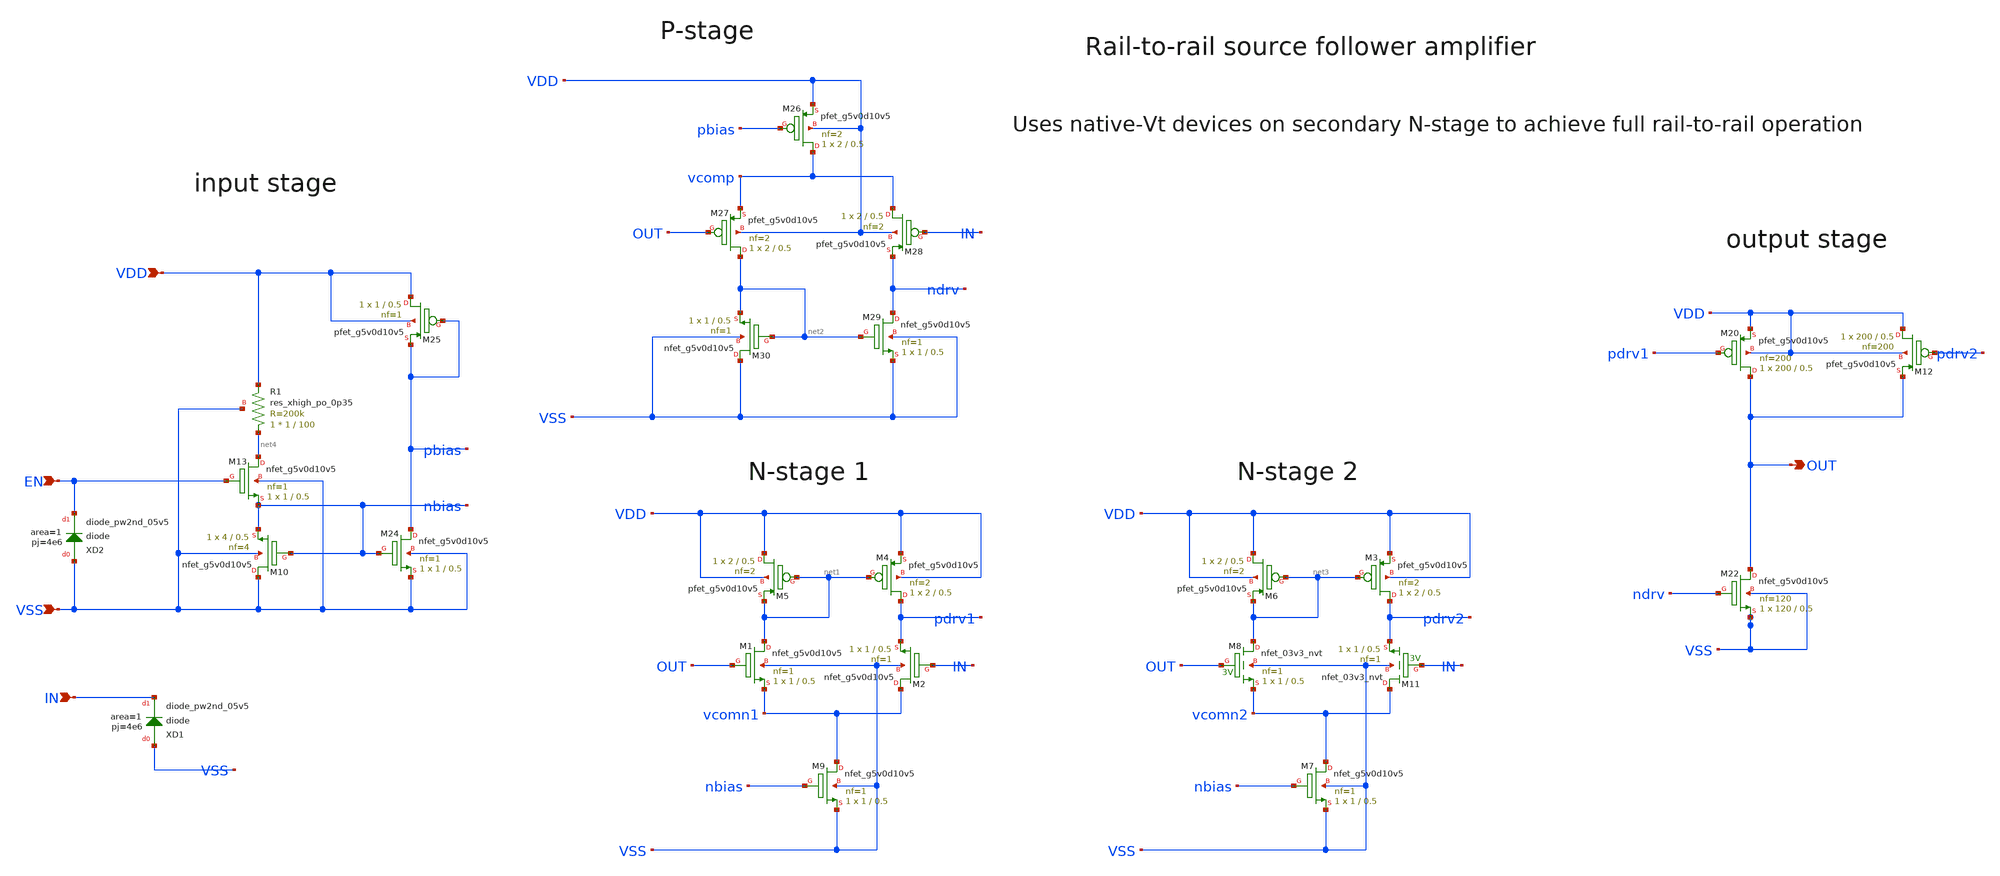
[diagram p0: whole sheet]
** sch_path: spice/xschem/EF_BUF3V3p.sch
**.subckt EF_BUF3V3p IN VDD VSS OUT EN
*.ipin IN
*.ipin VDD
*.ipin VSS
*.opin OUT
*.ipin EN
XM4 pdrv1 net1 VDD VDD sky130_fd_pr__pfet_g5v0d10v5 L=0.5 W=2 nf=2 ad='int((nf+1)/2) * W/nf * 0.29' as='int((nf+2)/2) * W/nf * 0.29'
+ pd='2*int((nf+1)/2) * (W/nf + 0.29)' ps='2*int((nf+2)/2) * (W/nf + 0.29)' nrd='0.29 / W' nrs='0.29 / W'
+ sa=0 sb=0 sd=0 mult=1 m=1
XM5 VDD net1 net1 VDD sky130_fd_pr__pfet_g5v0d10v5 L=0.5 W=2 nf=2 ad='int((nf+1)/2) * W/nf * 0.29' as='int((nf+2)/2) * W/nf * 0.29'
+ pd='2*int((nf+1)/2) * (W/nf + 0.29)' ps='2*int((nf+2)/2) * (W/nf + 0.29)' nrd='0.29 / W' nrs='0.29 / W'
+ sa=0 sb=0 sd=0 mult=1 m=1
XM9 vcomn1 nbias VSS VSS sky130_fd_pr__nfet_g5v0d10v5 L=0.5 W=1 nf=1 ad='int((nf+1)/2) * W/nf * 0.29'
+ as='int((nf+2)/2) * W/nf * 0.29' pd='2*int((nf+1)/2) * (W/nf + 0.29)' ps='2*int((nf+2)/2) * (W/nf + 0.29)'
+ nrd='0.29 / W' nrs='0.29 / W' sa=0 sb=0 sd=0 mult=1 m=1
XM10 VSS nbias nbias VSS sky130_fd_pr__nfet_g5v0d10v5 L=0.5 W=4 nf=4 ad='int((nf+1)/2) * W/nf * 0.29'
+ as='int((nf+2)/2) * W/nf * 0.29' pd='2*int((nf+1)/2) * (W/nf + 0.29)' ps='2*int((nf+2)/2) * (W/nf + 0.29)'
+ nrd='0.29 / W' nrs='0.29 / W' sa=0 sb=0 sd=0 mult=1 m=1
XR1 net4 VDD VSS sky130_fd_pr__res_xhigh_po_0p35 W=1 L=100 mult=1 m=1
XM20 OUT pdrv1 VDD VDD sky130_fd_pr__pfet_g5v0d10v5 L=0.5 W=200 nf=200 ad='int((nf+1)/2) * W/nf * 0.29'
+ as='int((nf+2)/2) * W/nf * 0.29' pd='2*int((nf+1)/2) * (W/nf + 0.29)' ps='2*int((nf+2)/2) * (W/nf + 0.29)'
+ nrd='0.29 / W' nrs='0.29 / W' sa=0 sb=0 sd=0 mult=1 m=1
XM22 OUT ndrv VSS VSS sky130_fd_pr__nfet_g5v0d10v5 L=0.5 W=120 nf=120 ad='int((nf+1)/2) * W/nf * 0.29'
+ as='int((nf+2)/2) * W/nf * 0.29' pd='2*int((nf+1)/2) * (W/nf + 0.29)' ps='2*int((nf+2)/2) * (W/nf + 0.29)'
+ nrd='0.29 / W' nrs='0.29 / W' sa=0 sb=0 sd=0 mult=1 m=1
XM24 pbias nbias VSS VSS sky130_fd_pr__nfet_g5v0d10v5 L=0.5 W=1 nf=1 ad='int((nf+1)/2) * W/nf * 0.29'
+ as='int((nf+2)/2) * W/nf * 0.29' pd='2*int((nf+1)/2) * (W/nf + 0.29)' ps='2*int((nf+2)/2) * (W/nf + 0.29)'
+ nrd='0.29 / W' nrs='0.29 / W' sa=0 sb=0 sd=0 mult=1 m=1
XM25 VDD pbias pbias VDD sky130_fd_pr__pfet_g5v0d10v5 L=0.5 W=1 nf=1 ad='int((nf+1)/2) * W/nf * 0.29'
+ as='int((nf+2)/2) * W/nf * 0.29' pd='2*int((nf+1)/2) * (W/nf + 0.29)' ps='2*int((nf+2)/2) * (W/nf + 0.29)'
+ nrd='0.29 / W' nrs='0.29 / W' sa=0 sb=0 sd=0 mult=1 m=1
XM26 vcomp pbias VDD VDD sky130_fd_pr__pfet_g5v0d10v5 L=0.5 W=2 nf=2 ad='int((nf+1)/2) * W/nf * 0.29'
+ as='int((nf+2)/2) * W/nf * 0.29' pd='2*int((nf+1)/2) * (W/nf + 0.29)' ps='2*int((nf+2)/2) * (W/nf + 0.29)'
+ nrd='0.29 / W' nrs='0.29 / W' sa=0 sb=0 sd=0 mult=1 m=1
XM27 net2 OUT vcomp VDD sky130_fd_pr__pfet_g5v0d10v5 L=0.5 W=2 nf=2 ad='int((nf+1)/2) * W/nf * 0.29'
+ as='int((nf+2)/2) * W/nf * 0.29' pd='2*int((nf+1)/2) * (W/nf + 0.29)' ps='2*int((nf+2)/2) * (W/nf + 0.29)'
+ nrd='0.29 / W' nrs='0.29 / W' sa=0 sb=0 sd=0 mult=1 m=1
XM28 vcomp IN ndrv VDD sky130_fd_pr__pfet_g5v0d10v5 L=0.5 W=2 nf=2 ad='int((nf+1)/2) * W/nf * 0.29' as='int((nf+2)/2) * W/nf * 0.29'
+ pd='2*int((nf+1)/2) * (W/nf + 0.29)' ps='2*int((nf+2)/2) * (W/nf + 0.29)' nrd='0.29 / W' nrs='0.29 / W'
+ sa=0 sb=0 sd=0 mult=1 m=1
XM29 ndrv net2 VSS VSS sky130_fd_pr__nfet_g5v0d10v5 L=0.5 W=1 nf=1 ad='int((nf+1)/2) * W/nf * 0.29' as='int((nf+2)/2) * W/nf * 0.29'
+ pd='2*int((nf+1)/2) * (W/nf + 0.29)' ps='2*int((nf+2)/2) * (W/nf + 0.29)' nrd='0.29 / W' nrs='0.29 / W'
+ sa=0 sb=0 sd=0 mult=1 m=1
XM30 VSS net2 net2 VSS sky130_fd_pr__nfet_g5v0d10v5 L=0.5 W=1 nf=1 ad='int((nf+1)/2) * W/nf * 0.29' as='int((nf+2)/2) * W/nf * 0.29'
+ pd='2*int((nf+1)/2) * (W/nf + 0.29)' ps='2*int((nf+2)/2) * (W/nf + 0.29)' nrd='0.29 / W' nrs='0.29 / W'
+ sa=0 sb=0 sd=0 mult=1 m=1
XM1 net1 OUT vcomn1 VSS sky130_fd_pr__nfet_g5v0d10v5 L=0.5 W=1 nf=1 ad='int((nf+1)/2) * W/nf * 0.29'
+ as='int((nf+2)/2) * W/nf * 0.29' pd='2*int((nf+1)/2) * (W/nf + 0.29)' ps='2*int((nf+2)/2) * (W/nf + 0.29)'
+ nrd='0.29 / W' nrs='0.29 / W' sa=0 sb=0 sd=0 mult=1 m=1
XM2 vcomn1 IN pdrv1 VSS sky130_fd_pr__nfet_g5v0d10v5 L=0.5 W=1 nf=1 ad='int((nf+1)/2) * W/nf * 0.29'
+ as='int((nf+2)/2) * W/nf * 0.29' pd='2*int((nf+1)/2) * (W/nf + 0.29)' ps='2*int((nf+2)/2) * (W/nf + 0.29)'
+ nrd='0.29 / W' nrs='0.29 / W' sa=0 sb=0 sd=0 mult=1 m=1
XM3 pdrv2 net3 VDD VDD sky130_fd_pr__pfet_g5v0d10v5 L=0.5 W=2 nf=2 ad='int((nf+1)/2) * W/nf * 0.29' as='int((nf+2)/2) * W/nf * 0.29'
+ pd='2*int((nf+1)/2) * (W/nf + 0.29)' ps='2*int((nf+2)/2) * (W/nf + 0.29)' nrd='0.29 / W' nrs='0.29 / W'
+ sa=0 sb=0 sd=0 mult=1 m=1
XM6 VDD net3 net3 VDD sky130_fd_pr__pfet_g5v0d10v5 L=0.5 W=2 nf=2 ad='int((nf+1)/2) * W/nf * 0.29' as='int((nf+2)/2) * W/nf * 0.29'
+ pd='2*int((nf+1)/2) * (W/nf + 0.29)' ps='2*int((nf+2)/2) * (W/nf + 0.29)' nrd='0.29 / W' nrs='0.29 / W'
+ sa=0 sb=0 sd=0 mult=1 m=1
XM7 vcomn2 nbias VSS VSS sky130_fd_pr__nfet_g5v0d10v5 L=0.5 W=1 nf=1 ad='int((nf+1)/2) * W/nf * 0.29'
+ as='int((nf+2)/2) * W/nf * 0.29' pd='2*int((nf+1)/2) * (W/nf + 0.29)' ps='2*int((nf+2)/2) * (W/nf + 0.29)'
+ nrd='0.29 / W' nrs='0.29 / W' sa=0 sb=0 sd=0 mult=1 m=1
XM8 net3 OUT vcomn2 VSS sky130_fd_pr__nfet_03v3_nvt L=0.5 W=1 nf=1 ad='int((nf+1)/2) * W/nf * 0.29' as='int((nf+2)/2) * W/nf * 0.29'
+ pd='2*int((nf+1)/2) * (W/nf + 0.29)' ps='2*int((nf+2)/2) * (W/nf + 0.29)' nrd='0.29 / W' nrs='0.29 / W'
+ sa=0 sb=0 sd=0 mult=1 m=1
XM11 vcomn2 IN pdrv2 VSS sky130_fd_pr__nfet_03v3_nvt L=0.5 W=1 nf=1 ad='int((nf+1)/2) * W/nf * 0.29'
+ as='int((nf+2)/2) * W/nf * 0.29' pd='2*int((nf+1)/2) * (W/nf + 0.29)' ps='2*int((nf+2)/2) * (W/nf + 0.29)'
+ nrd='0.29 / W' nrs='0.29 / W' sa=0 sb=0 sd=0 mult=1 m=1
XM12 VDD pdrv2 OUT VDD sky130_fd_pr__pfet_g5v0d10v5 L=0.5 W=200 nf=200 ad='int((nf+1)/2) * W/nf * 0.29'
+ as='int((nf+2)/2) * W/nf * 0.29' pd='2*int((nf+1)/2) * (W/nf + 0.29)' ps='2*int((nf+2)/2) * (W/nf + 0.29)'
+ nrd='0.29 / W' nrs='0.29 / W' sa=0 sb=0 sd=0 mult=1 m=1
XXD1 VSS IN sky130_fd_pr__diode_pw2nd_05v5 area=1 pj=4e6
XM13 net4 EN nbias VSS sky130_fd_pr__nfet_g5v0d10v5 L=0.5 W=1 nf=1 ad='int((nf+1)/2) * W/nf * 0.29' as='int((nf+2)/2) * W/nf * 0.29'
+ pd='2*int((nf+1)/2) * (W/nf + 0.29)' ps='2*int((nf+2)/2) * (W/nf + 0.29)' nrd='0.29 / W' nrs='0.29 / W'
+ sa=0 sb=0 sd=0 mult=1 m=1
XXD2 VSS EN sky130_fd_pr__diode_pw2nd_05v5 area=1 pj=4e6
**.ends
.end
